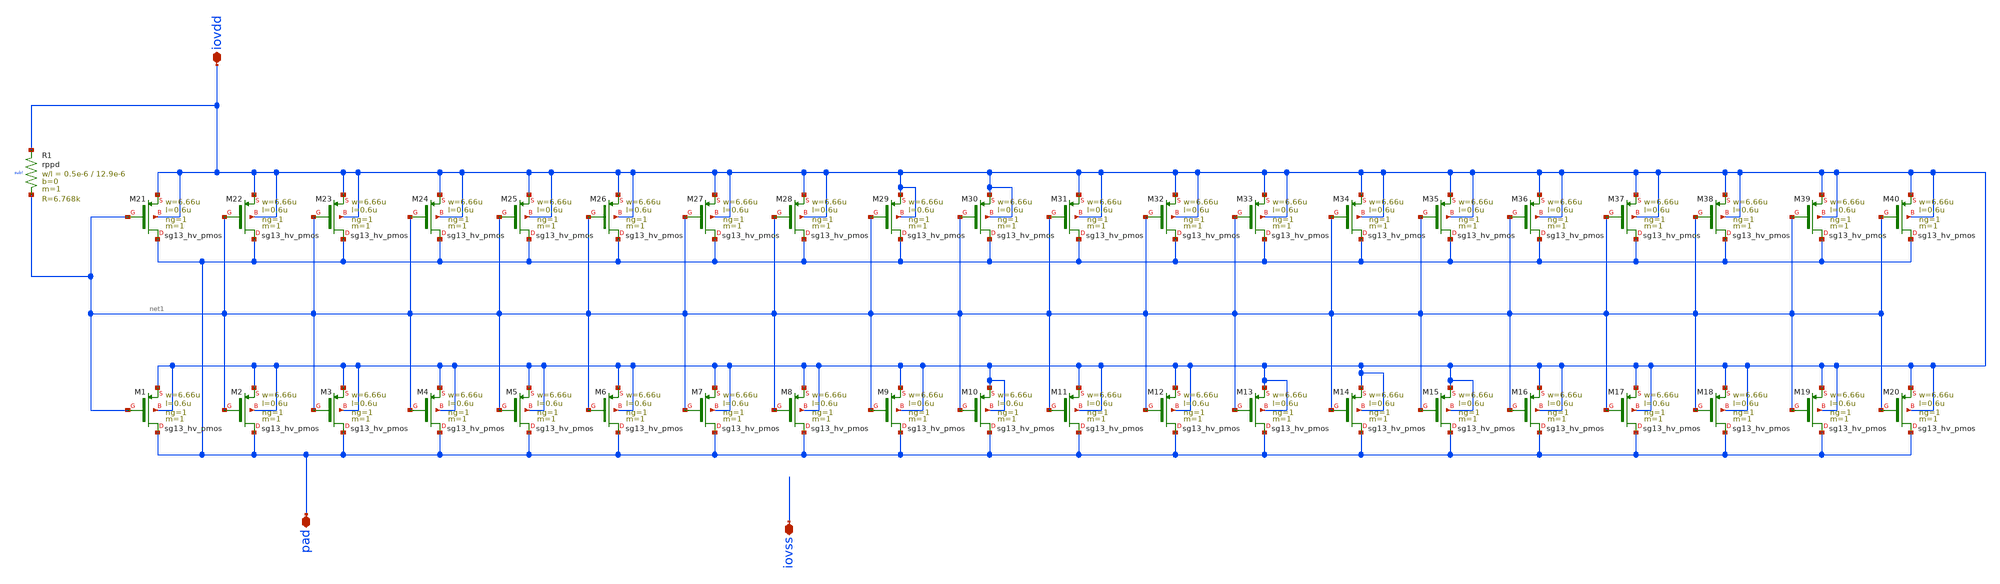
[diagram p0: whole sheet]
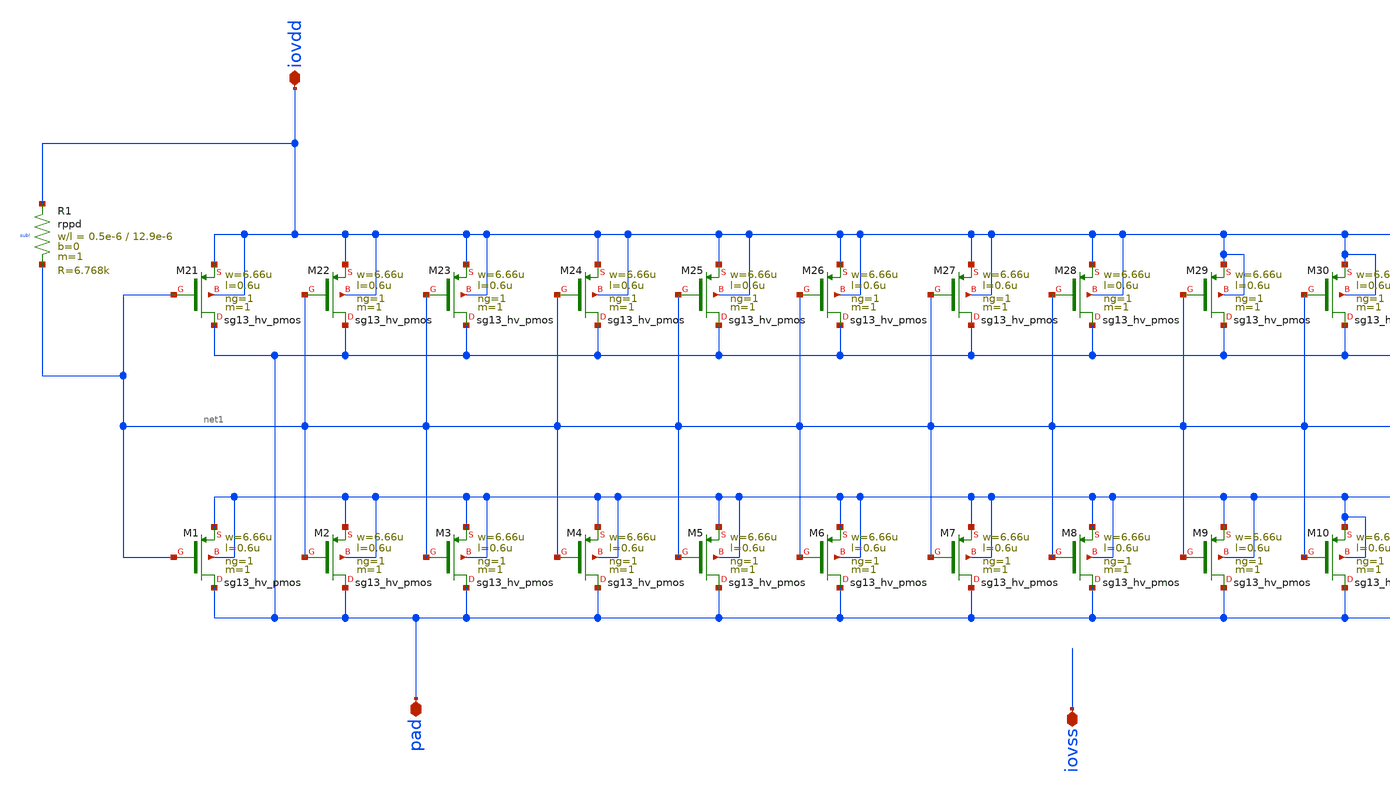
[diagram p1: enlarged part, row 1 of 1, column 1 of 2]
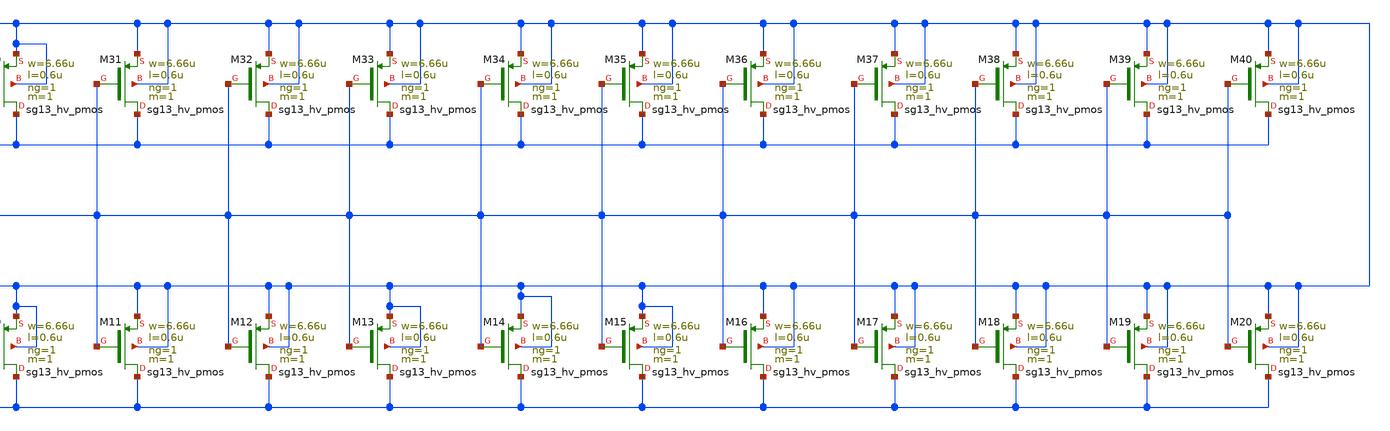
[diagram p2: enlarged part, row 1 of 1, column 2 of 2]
** sch_path: ihp-sg13g2/libs.ref/sg13g2_io/xschem/sg13g2_Clamp_P20N0D.sch
**.subckt sg13g2_Clamp_P20N0D iovdd pad iovss
*.iopin iovdd
*.iopin pad
*.iopin iovss
XM1 pad net1 iovdd iovdd sg13_hv_pmos w=6.66u l=0.6u ng=1 m=1 mm_ok=1
XM2 pad net1 iovdd iovdd sg13_hv_pmos w=6.66u l=0.6u ng=1 m=1 mm_ok=1
XM3 pad net1 iovdd iovdd sg13_hv_pmos w=6.66u l=0.6u ng=1 m=1 mm_ok=1
XM4 pad net1 iovdd iovdd sg13_hv_pmos w=6.66u l=0.6u ng=1 m=1 mm_ok=1
XM5 pad net1 iovdd iovdd sg13_hv_pmos w=6.66u l=0.6u ng=1 m=1 mm_ok=1
XM6 pad net1 iovdd iovdd sg13_hv_pmos w=6.66u l=0.6u ng=1 m=1 mm_ok=1
XM7 pad net1 iovdd iovdd sg13_hv_pmos w=6.66u l=0.6u ng=1 m=1 mm_ok=1
XM8 pad net1 iovdd iovdd sg13_hv_pmos w=6.66u l=0.6u ng=1 m=1 mm_ok=1
XM9 pad net1 iovdd iovdd sg13_hv_pmos w=6.66u l=0.6u ng=1 m=1 mm_ok=1
XM10 pad net1 iovdd iovdd sg13_hv_pmos w=6.66u l=0.6u ng=1 m=1 mm_ok=1
XM11 pad net1 iovdd iovdd sg13_hv_pmos w=6.66u l=0.6u ng=1 m=1 mm_ok=1
XM12 pad net1 iovdd iovdd sg13_hv_pmos w=6.66u l=0.6u ng=1 m=1 mm_ok=1
XM13 pad net1 iovdd iovdd sg13_hv_pmos w=6.66u l=0.6u ng=1 m=1 mm_ok=1
XM14 pad net1 iovdd iovdd sg13_hv_pmos w=6.66u l=0.6u ng=1 m=1 mm_ok=1
XM15 pad net1 iovdd iovdd sg13_hv_pmos w=6.66u l=0.6u ng=1 m=1 mm_ok=1
XM16 pad net1 iovdd iovdd sg13_hv_pmos w=6.66u l=0.6u ng=1 m=1 mm_ok=1
XM17 pad net1 iovdd iovdd sg13_hv_pmos w=6.66u l=0.6u ng=1 m=1 mm_ok=1
XM18 pad net1 iovdd iovdd sg13_hv_pmos w=6.66u l=0.6u ng=1 m=1 mm_ok=1
XM19 pad net1 iovdd iovdd sg13_hv_pmos w=6.66u l=0.6u ng=1 m=1 mm_ok=1
XM20 pad net1 iovdd iovdd sg13_hv_pmos w=6.66u l=0.6u ng=1 m=1 mm_ok=1
XM21 pad net1 iovdd iovdd sg13_hv_pmos w=6.66u l=0.6u ng=1 m=1 mm_ok=1
XM22 pad net1 iovdd iovdd sg13_hv_pmos w=6.66u l=0.6u ng=1 m=1 mm_ok=1
XM23 pad net1 iovdd iovdd sg13_hv_pmos w=6.66u l=0.6u ng=1 m=1 mm_ok=1
XM24 pad net1 iovdd iovdd sg13_hv_pmos w=6.66u l=0.6u ng=1 m=1 mm_ok=1
XM25 pad net1 iovdd iovdd sg13_hv_pmos w=6.66u l=0.6u ng=1 m=1 mm_ok=1
XM26 pad net1 iovdd iovdd sg13_hv_pmos w=6.66u l=0.6u ng=1 m=1 mm_ok=1
XM27 pad net1 iovdd iovdd sg13_hv_pmos w=6.66u l=0.6u ng=1 m=1 mm_ok=1
XM28 pad net1 iovdd iovdd sg13_hv_pmos w=6.66u l=0.6u ng=1 m=1 mm_ok=1
XM29 pad net1 iovdd iovdd sg13_hv_pmos w=6.66u l=0.6u ng=1 m=1 mm_ok=1
XM30 pad net1 iovdd iovdd sg13_hv_pmos w=6.66u l=0.6u ng=1 m=1 mm_ok=1
XM31 pad net1 iovdd iovdd sg13_hv_pmos w=6.66u l=0.6u ng=1 m=1 mm_ok=1
XM32 pad net1 iovdd iovdd sg13_hv_pmos w=6.66u l=0.6u ng=1 m=1 mm_ok=1
XM33 pad net1 iovdd iovdd sg13_hv_pmos w=6.66u l=0.6u ng=1 m=1 mm_ok=1
XM34 pad net1 iovdd iovdd sg13_hv_pmos w=6.66u l=0.6u ng=1 m=1 mm_ok=1
XM35 pad net1 iovdd iovdd sg13_hv_pmos w=6.66u l=0.6u ng=1 m=1 mm_ok=1
XM36 pad net1 iovdd iovdd sg13_hv_pmos w=6.66u l=0.6u ng=1 m=1 mm_ok=1
XM37 pad net1 iovdd iovdd sg13_hv_pmos w=6.66u l=0.6u ng=1 m=1 mm_ok=1
XM38 pad net1 iovdd iovdd sg13_hv_pmos w=6.66u l=0.6u ng=1 m=1 mm_ok=1
XM39 pad net1 iovdd iovdd sg13_hv_pmos w=6.66u l=0.6u ng=1 m=1 mm_ok=1
XM40 pad net1 iovdd iovdd sg13_hv_pmos w=6.66u l=0.6u ng=1 m=1 mm_ok=1
XR1 iovdd net1 sub! rppd w=0.5e-6 l=12.9e-6 m=1 b=0 mm_ok=1
**.ends
.end
